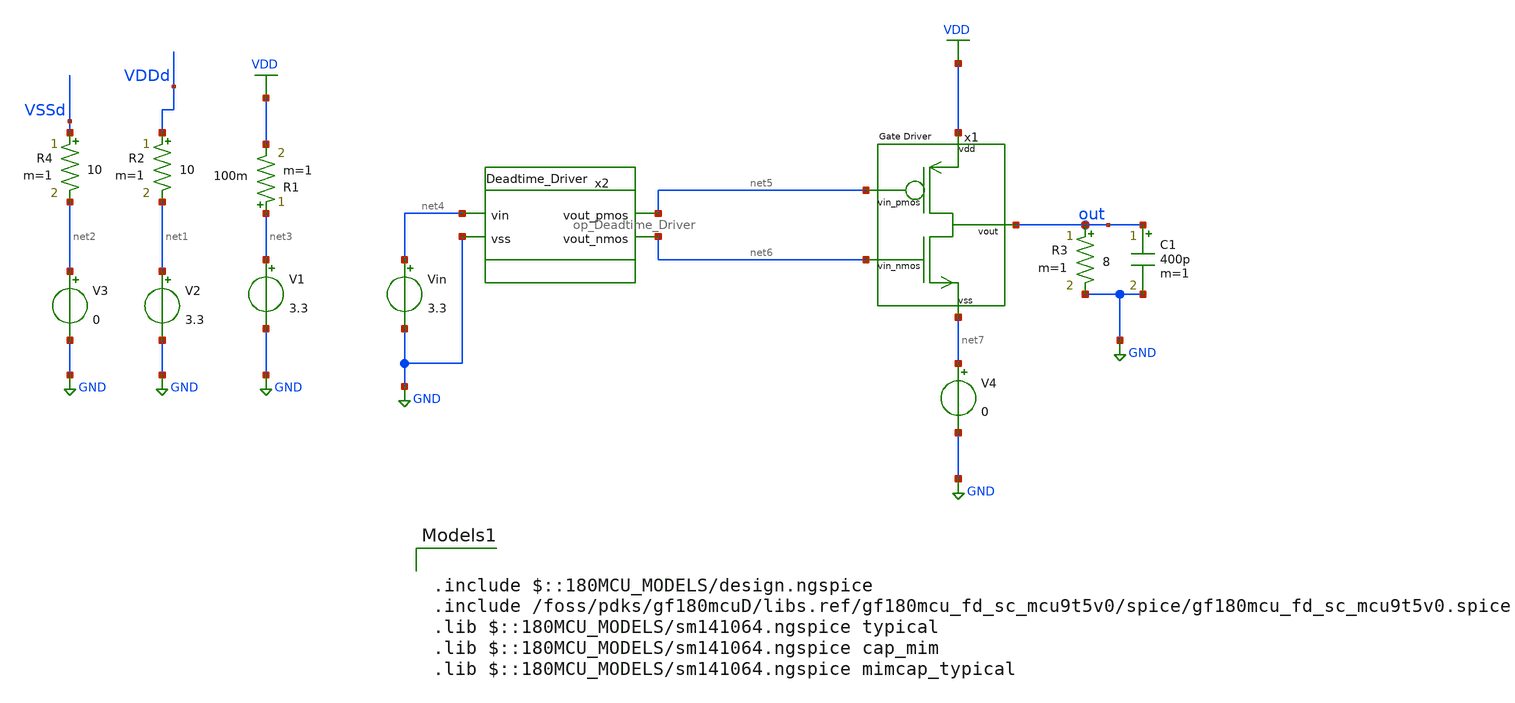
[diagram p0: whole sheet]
** sch_path: designs/libs/tb_analog/tb_Output_Stage/tb_test_output.sch
**.subckt tb_test_output
V2 net1 GND 3.3
R2 VDDd net1 10 m=1
V3 net2 GND 0
R4 VSSd net2 10 m=1
V1 net3 GND 3.3
R1 net3 VDD 100m m=1
Vin net4 GND 3.3
x1 VDD net5 out net6 net7 Output_Stage
x2 net5 net4 net6 GND op_Deadtime_Driver
R3 out GND 8 m=1
C1 out GND 400p m=1
V4 net7 GND 0
**** begin user architecture code

.include $::180MCU_MODELS/design.ngspice
.include /foss/pdks/gf180mcuD/libs.ref/gf180mcu_fd_sc_mcu9t5v0/spice/gf180mcu_fd_sc_mcu9t5v0.spice
.lib $::180MCU_MODELS/sm141064.ngspice typical
.lib $::180MCU_MODELS/sm141064.ngspice cap_mim
.lib $::180MCU_MODELS/sm141064.ngspice mimcap_typical



.temp 27
.options savecurrents
.global VDDd VSSd
.control
save all
**Frequency & time settings
let fsig = 20k
let tper=1/fsig
let tfr = 0.01*tper
let ton = 0.5*tper-2*tfr

let tstop = 4 * tper
let tstep = 0.001*tper


**voltages
alter @Vin[PULSE] = [ 0 2.3 0 $&tfr $&tfr $&ton $&tper 3 ]
alter @Vin[DC] = 3.3
*alter @Vin[SIN] = [ 1.7 1.5 $&fsig 0 0 ]

**simulation
OP
*show all > op.log
show all

**Temperature analysis
tran $&tstep $&tstop
let t = $temp
print t
*plot nmos pmos
plot out
meas tran tfall_p WHEN v(pmos)=0.68 FALL=3
meas tran tfall_n WHEN v(nmos)=0.68 FALL=3

meas tran trise_p WHEN v(pmos)=0.68 RISE=3
meas tran trise_n WHEN v(nmos)=0.68 RISE=3

let delay_fall = $&tfall_p - $&tfall_n
let delay_rise = $&trise_p - $&trise_n

print delay_fall
print delay_rise

**check shoot-through
plot @r5[i] v3#branch v4#branch

*@m.xm1.m0[id]
*plot @m.xm1.m0[id]

plot v4#branch

meas tran v_max MAX v(out)
meas tran v_min MIN v(out)
let vpp = $&v_max - $&v_min
print vpp
write Deadtime_Driver_temp_tb.txt
.endc


**** end user architecture code
**.ends
.GLOBAL GND
.GLOBAL VDD
.end
